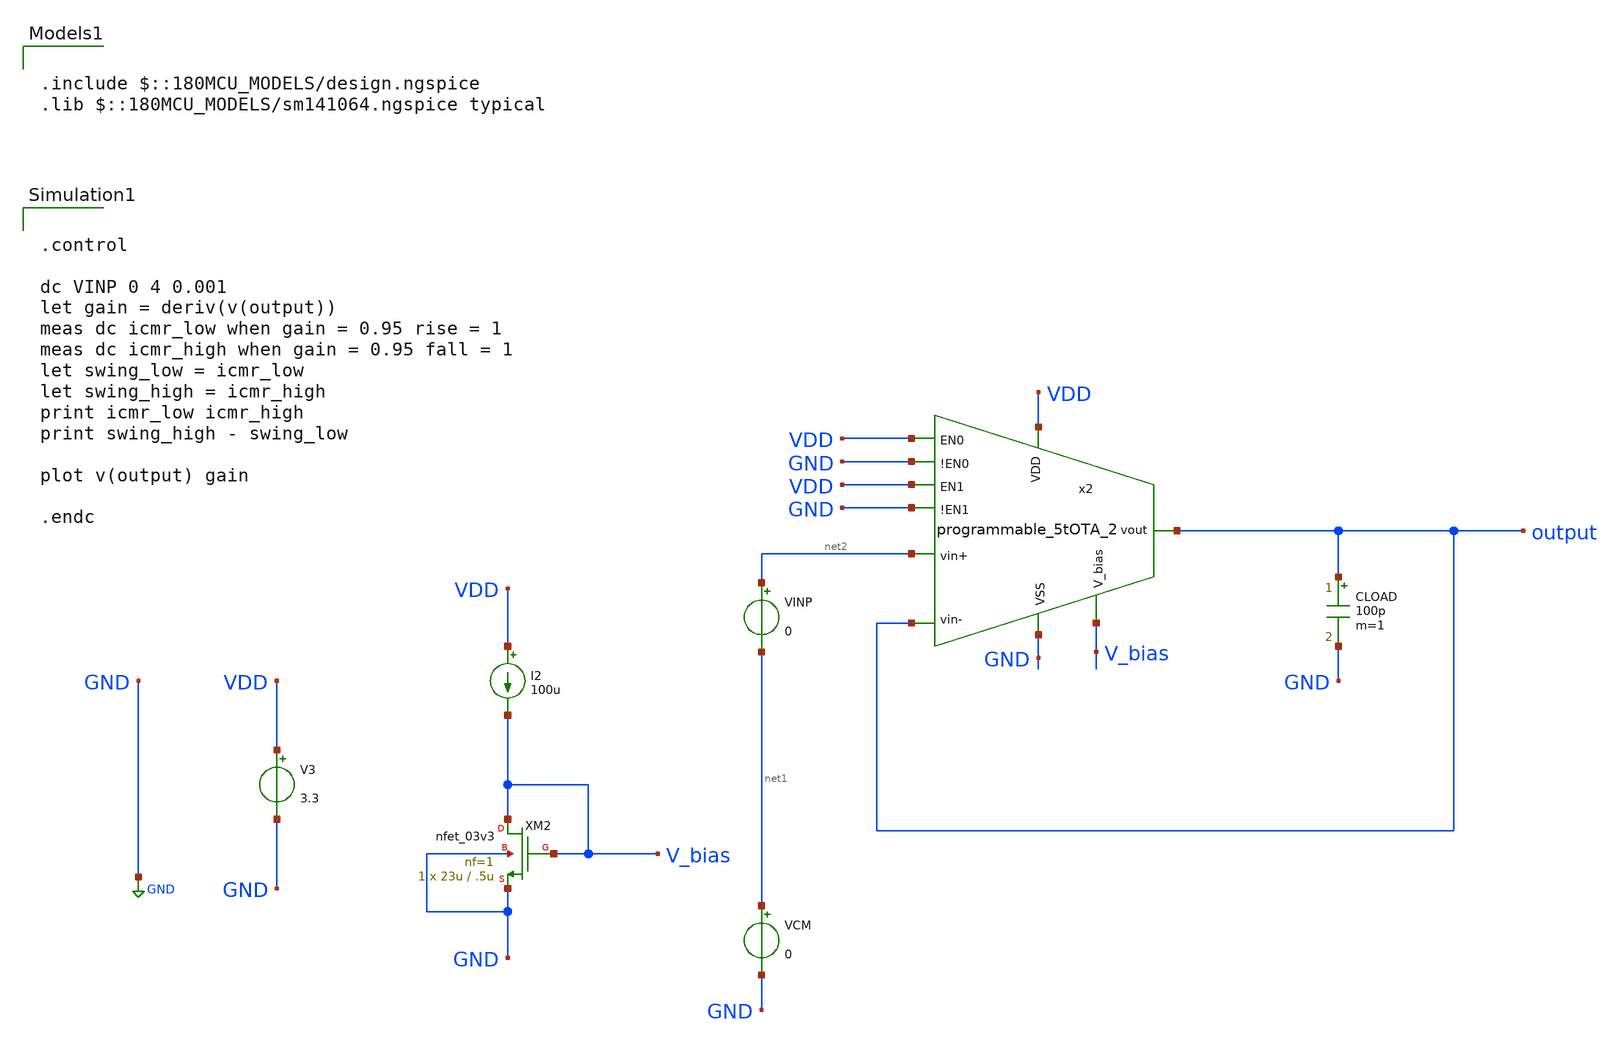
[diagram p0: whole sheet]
** sch_path: designs/libs/core_amps/ota_5t/programmable_5tOTA_op_2.sch
**.subckt programmable_5tOTA_op_2
XM2 V_bias V_bias GND GND nfet_03v3 L=.5u W=23u nf=1 ad='int((nf+1)/2) * W/nf * 0.18u' as='int((nf+2)/2) * W/nf * 0.18u'
+ pd='2*int((nf+1)/2) * (W/nf + 0.18u)' ps='2*int((nf+2)/2) * (W/nf + 0.18u)' nrd='0.18u / W' nrs='0.18u / W'
+ sa=0 sb=0 sd=0 m=1
I2 VDD V_bias 100u
V3 VDD GND 3.3
CLOAD output GND 100p m=1
VINP net2 net1 0
VCM net1 GND 0
x2 VDD VDD GND output VDD GND output net2 V_bias GND programmable_5tOTA_2
**** begin user architecture code

.include $::180MCU_MODELS/design.ngspice
.lib $::180MCU_MODELS/sm141064.ngspice typical



.control

dc VINP 0 4 0.001
let gain = deriv(v(output))
meas dc icmr_low when gain = 0.95 rise = 1
meas dc icmr_high when gain = 0.95 fall = 1
let swing_low = icmr_low
let swing_high = icmr_high
print icmr_low icmr_high
print swing_high - swing_low

plot v(output) gain

.endc


**** end user architecture code
**.ends
.GLOBAL GND
.end
